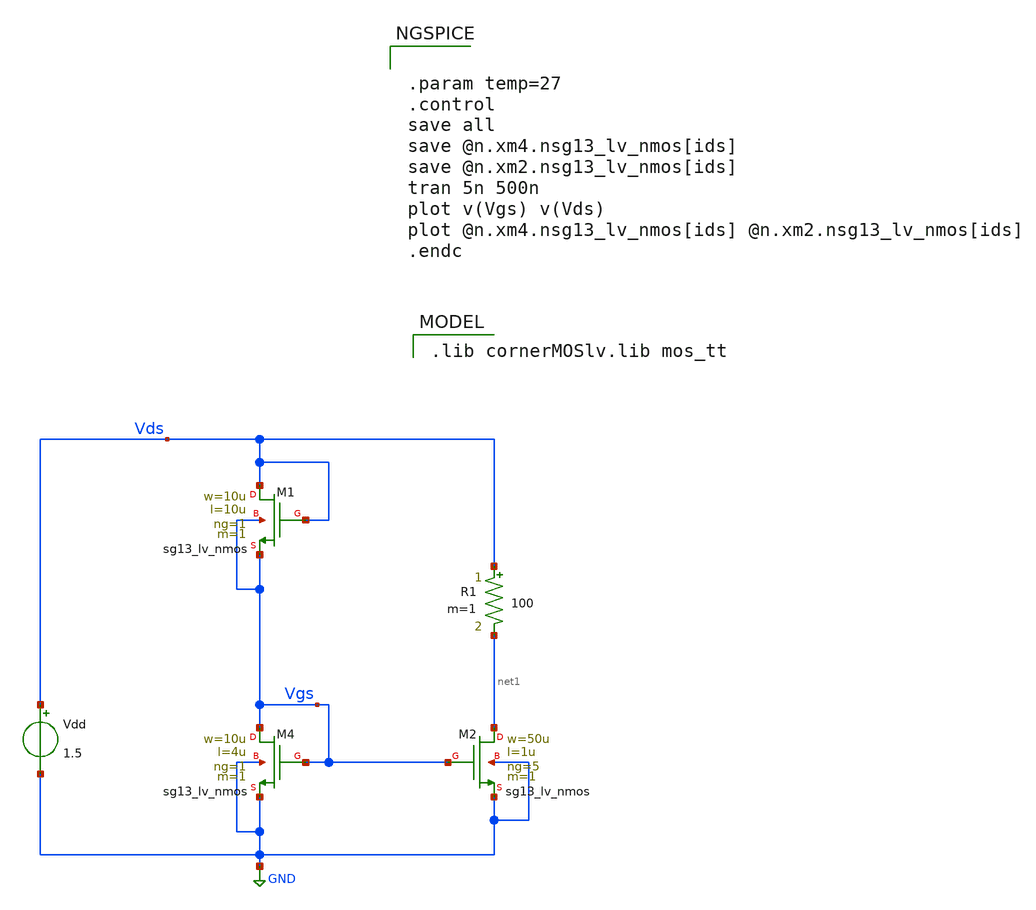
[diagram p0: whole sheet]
** sch_path: xschem/mosfet_diode.sch
**.subckt mosfet_diode
XM4 Vgs Vgs GND GND sg13_lv_nmos w=10u l=4u ng=1 m=1 mm_ok=1
Vdd Vds GND 1.5
XM1 Vds Vds Vgs Vgs sg13_lv_nmos w=10u l=10u ng=1 m=1 mm_ok=1
XM2 net1 Vgs GND GND sg13_lv_nmos w=50u l=1u ng=5 m=1 mm_ok=1
R1 Vds net1 100 m=1
**** begin user architecture code


.param temp=27
.control
save all
save @n.xm4.nsg13_lv_nmos[ids]
save @n.xm2.nsg13_lv_nmos[ids]
tran 5n 500n
plot v(Vgs) v(Vds)
plot @n.xm4.nsg13_lv_nmos[ids] @n.xm2.nsg13_lv_nmos[ids]
.endc


 .lib cornerMOSlv.lib mos_tt

**** end user architecture code
**.ends
.GLOBAL GND
.end
